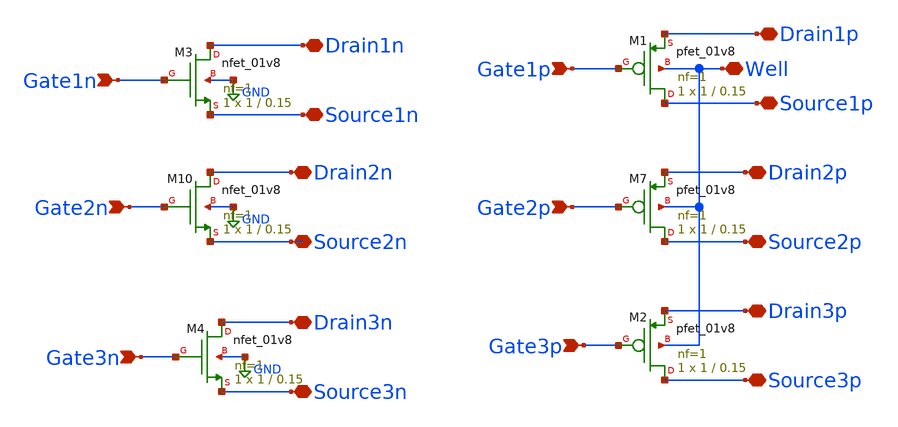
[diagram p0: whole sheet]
** sch_path: libs.ref/sky130_hilas_sc/xschem/sky130_hilas_Trans4small.sch
**.subckt sky130_hilas_Trans4small Gate2n Well Source2p Gate1n Drain1n Source3p Gate3p Drain3n
*+ Drain2n Gate2p Source1p Gate1p Gate3n Drain1p Drain3p Drain2p Source2n Source3n Source1n
*.ipin Gate2n
*.iopin Well
*.iopin Source2p
*.ipin Gate1n
*.iopin Drain1n
*.iopin Source3p
*.ipin Gate3p
*.iopin Drain3n
*.iopin Drain2n
*.ipin Gate2p
*.iopin Source1p
*.ipin Gate1p
*.ipin Gate3n
*.iopin Drain1p
*.iopin Drain3p
*.iopin Drain2p
*.iopin Source2n
*.iopin Source3n
*.iopin Source1n
XM1 Source1p Gate1p Drain1p Well sky130_fd_pr__pfet_01v8 L=0.15 W=1 nf=1 ad='int((nf+1)/2) * W/nf * 0.29'
+ as='int((nf+2)/2) * W/nf * 0.29' pd='2*int((nf+1)/2) * (W/nf + 0.29)' ps='2*int((nf+2)/2) * (W/nf + 0.29)'
+ nrd='0.29 / W' nrs='0.29 / W' sa=0 sb=0 sd=0 mult=1 m=1
XM2 Source3p Gate3p Drain3p Well sky130_fd_pr__pfet_01v8 L=0.15 W=1 nf=1 ad='int((nf+1)/2) * W/nf * 0.29'
+ as='int((nf+2)/2) * W/nf * 0.29' pd='2*int((nf+1)/2) * (W/nf + 0.29)' ps='2*int((nf+2)/2) * (W/nf + 0.29)'
+ nrd='0.29 / W' nrs='0.29 / W' sa=0 sb=0 sd=0 mult=1 m=1
XM3 Drain1n Gate1n Source1n GND sky130_fd_pr__nfet_01v8 L=0.15 W=1 nf=1 ad='int((nf+1)/2) * W/nf * 0.29'
+ as='int((nf+2)/2) * W/nf * 0.29' pd='2*int((nf+1)/2) * (W/nf + 0.29)' ps='2*int((nf+2)/2) * (W/nf + 0.29)'
+ nrd='0.29 / W' nrs='0.29 / W' sa=0 sb=0 sd=0 mult=1 m=1
XM4 Drain3n Gate3n Source3n GND sky130_fd_pr__nfet_01v8 L=0.15 W=1 nf=1 ad='int((nf+1)/2) * W/nf * 0.29'
+ as='int((nf+2)/2) * W/nf * 0.29' pd='2*int((nf+1)/2) * (W/nf + 0.29)' ps='2*int((nf+2)/2) * (W/nf + 0.29)'
+ nrd='0.29 / W' nrs='0.29 / W' sa=0 sb=0 sd=0 mult=1 m=1
XM7 Source2p Gate2p Drain2p Well sky130_fd_pr__pfet_01v8 L=0.15 W=1 nf=1 ad='int((nf+1)/2) * W/nf * 0.29'
+ as='int((nf+2)/2) * W/nf * 0.29' pd='2*int((nf+1)/2) * (W/nf + 0.29)' ps='2*int((nf+2)/2) * (W/nf + 0.29)'
+ nrd='0.29 / W' nrs='0.29 / W' sa=0 sb=0 sd=0 mult=1 m=1
XM10 Drain2n Gate2n Source2n GND sky130_fd_pr__nfet_01v8 L=0.15 W=1 nf=1 ad='int((nf+1)/2) * W/nf * 0.29'
+ as='int((nf+2)/2) * W/nf * 0.29' pd='2*int((nf+1)/2) * (W/nf + 0.29)' ps='2*int((nf+2)/2) * (W/nf + 0.29)'
+ nrd='0.29 / W' nrs='0.29 / W' sa=0 sb=0 sd=0 mult=1 m=1
**.ends
.GLOBAL GND
.end
